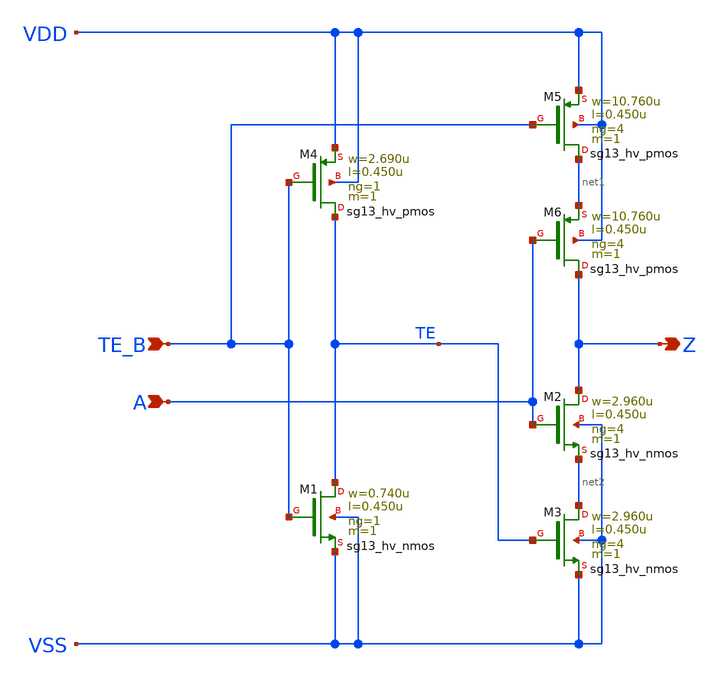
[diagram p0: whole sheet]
** sch_path: ihp-sg13g2/libs.ref/sg13g2_stdcell_hv/sch/xschem/sg13g2_hv_einvn_4.sch
* Copyright 2023 IHP PDK Authors
* Licensed under the Apache License, Version 2.0 (the "License");
* you may not use this file except in compliance with the License.
* You may obtain a copy of the License at
* https://www.apache.org/licenses/LICENSE-2.0
* Unless required by applicable law or agreed to in writing, software
* distributed under the License is distributed on an "AS IS" BASIS,
* WITHOUT WARRANTIES OR CONDITIONS OF ANY KIND, either express or implied.
* See the License for the specific language governing permissions and
* limitations under the License.
**.subckt sg13g2_hv_einvn_4 TE_B A Z
*.ipin TE_B
*.ipin A
*.opin Z
XM1 TE TE_B VSS VSS sg13_hv_nmos w=0.740u l=0.450u ng=1 m=1 mm_ok=1
XM2 Z A net2 VSS sg13_hv_nmos w=2.960u l=0.450u ng=4 m=1 mm_ok=1
XM3 net2 TE VSS VSS sg13_hv_nmos w=2.960u l=0.450u ng=4 m=1 mm_ok=1
XM4 TE TE_B VDD VDD sg13_hv_pmos w=2.690u l=0.450u ng=1 m=1 mm_ok=1
XM5 net1 TE_B VDD VDD sg13_hv_pmos w=10.760u l=0.450u ng=4 m=1 mm_ok=1
XM6 Z A net1 VDD sg13_hv_pmos w=10.760u l=0.450u ng=4 m=1 mm_ok=1
**.ends
.end
